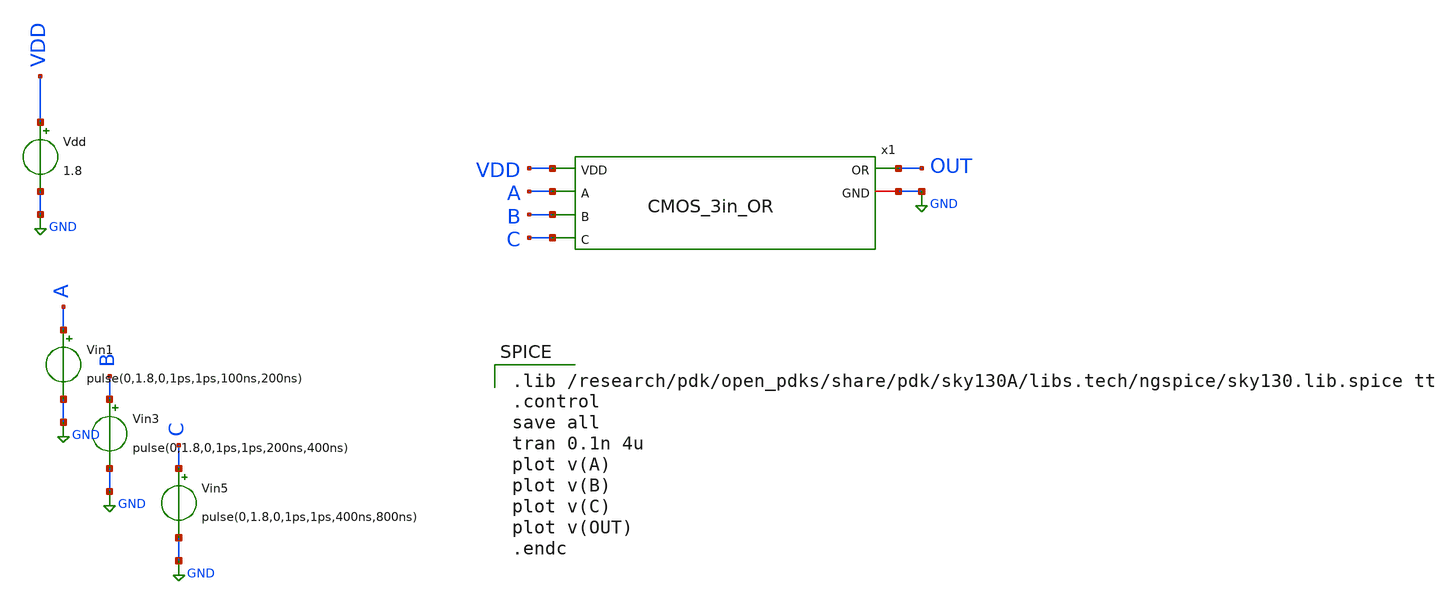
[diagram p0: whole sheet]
** sch_path: skywater_stuff/CMOS_3in_OR_sim.sch
**.subckt CMOS_3in_OR_sim
Vin1 A GND pulse(0,1.8,0,1ps,1ps,100ns,200ns)
Vin3 B GND pulse(0,1.8,0,1ps,1ps,200ns,400ns)
Vin5 C GND pulse(0,1.8,0,1ps,1ps,400ns,800ns)
Vdd VDD GND 1.8
x1 A B C OUT GND VDD CMOS_3in_OR
**** begin user architecture code

.lib /research/pdk/open_pdks/share/pdk/sky130A/libs.tech/ngspice/sky130.lib.spice tt
.control
save all
tran 0.1n 4u
plot v(A)
plot v(B)
plot v(C)
plot v(OUT)
.endc


**** end user architecture code
**.ends

* expanding   symbol:  CMOS_3in_OR.sym # of pins=6
** sym_path: skywater_stuff/CMOS_3in_OR.sym
** sch_path: skywater_stuff/CMOS_3in_OR.sch
.subckt CMOS_3in_OR A B C OR GND VDD
*.ipin A
*.ipin B
*.ipin C
*.opin OR
*.iopin GND
*.ipin VDD
XM4 net2 A VDD VDD sky130_fd_pr__pfet_01v8 L=0.15 W=3 nf=1 ad='int((nf+1)/2) * W/nf * 0.29' as='int((nf+2)/2) * W/nf * 0.29'
+ pd='2*int((nf+1)/2) * (W/nf + 0.29)' ps='2*int((nf+2)/2) * (W/nf + 0.29)' nrd='0.29 / W' nrs='0.29 / W'
+ sa=0 sb=0 sd=0 mult=1 m=1
XM2 net3 B net2 VDD sky130_fd_pr__pfet_01v8 L=0.15 W=3 nf=1 ad='int((nf+1)/2) * W/nf * 0.29' as='int((nf+2)/2) * W/nf * 0.29'
+ pd='2*int((nf+1)/2) * (W/nf + 0.29)' ps='2*int((nf+2)/2) * (W/nf + 0.29)' nrd='0.29 / W' nrs='0.29 / W'
+ sa=0 sb=0 sd=0 mult=1 m=1
XM5 OR net1 GND GND sky130_fd_pr__nfet_01v8 L=0.15 W=1.5 nf=1 ad='int((nf+1)/2) * W/nf * 0.29' as='int((nf+2)/2) * W/nf * 0.29'
+ pd='2*int((nf+1)/2) * (W/nf + 0.29)' ps='2*int((nf+2)/2) * (W/nf + 0.29)' nrd='0.29 / W' nrs='0.29 / W'
+ sa=0 sb=0 sd=0 mult=1 m=1
XM1 net1 B GND GND sky130_fd_pr__nfet_01v8 L=0.15 W=1.5 nf=1 ad='int((nf+1)/2) * W/nf * 0.29' as='int((nf+2)/2) * W/nf * 0.29'
+ pd='2*int((nf+1)/2) * (W/nf + 0.29)' ps='2*int((nf+2)/2) * (W/nf + 0.29)' nrd='0.29 / W' nrs='0.29 / W'
+ sa=0 sb=0 sd=0 mult=1 m=1
XM6 OR net1 VDD VDD sky130_fd_pr__pfet_01v8 L=0.15 W=3 nf=1 ad='int((nf+1)/2) * W/nf * 0.29' as='int((nf+2)/2) * W/nf * 0.29'
+ pd='2*int((nf+1)/2) * (W/nf + 0.29)' ps='2*int((nf+2)/2) * (W/nf + 0.29)' nrd='0.29 / W' nrs='0.29 / W'
+ sa=0 sb=0 sd=0 mult=1 m=1
XM7 net1 C GND GND sky130_fd_pr__nfet_01v8 L=0.15 W=1.5 nf=1 ad='int((nf+1)/2) * W/nf * 0.29' as='int((nf+2)/2) * W/nf * 0.29'
+ pd='2*int((nf+1)/2) * (W/nf + 0.29)' ps='2*int((nf+2)/2) * (W/nf + 0.29)' nrd='0.29 / W' nrs='0.29 / W'
+ sa=0 sb=0 sd=0 mult=1 m=1
XM3 net1 A GND GND sky130_fd_pr__nfet_01v8 L=0.15 W=1.5 nf=1 ad='int((nf+1)/2) * W/nf * 0.29' as='int((nf+2)/2) * W/nf * 0.29'
+ pd='2*int((nf+1)/2) * (W/nf + 0.29)' ps='2*int((nf+2)/2) * (W/nf + 0.29)' nrd='0.29 / W' nrs='0.29 / W'
+ sa=0 sb=0 sd=0 mult=1 m=1
XM8 net1 C net3 VDD sky130_fd_pr__pfet_01v8 L=0.15 W=3 nf=1 ad='int((nf+1)/2) * W/nf * 0.29' as='int((nf+2)/2) * W/nf * 0.29'
+ pd='2*int((nf+1)/2) * (W/nf + 0.29)' ps='2*int((nf+2)/2) * (W/nf + 0.29)' nrd='0.29 / W' nrs='0.29 / W'
+ sa=0 sb=0 sd=0 mult=1 m=1
.ends

.GLOBAL GND
.end
